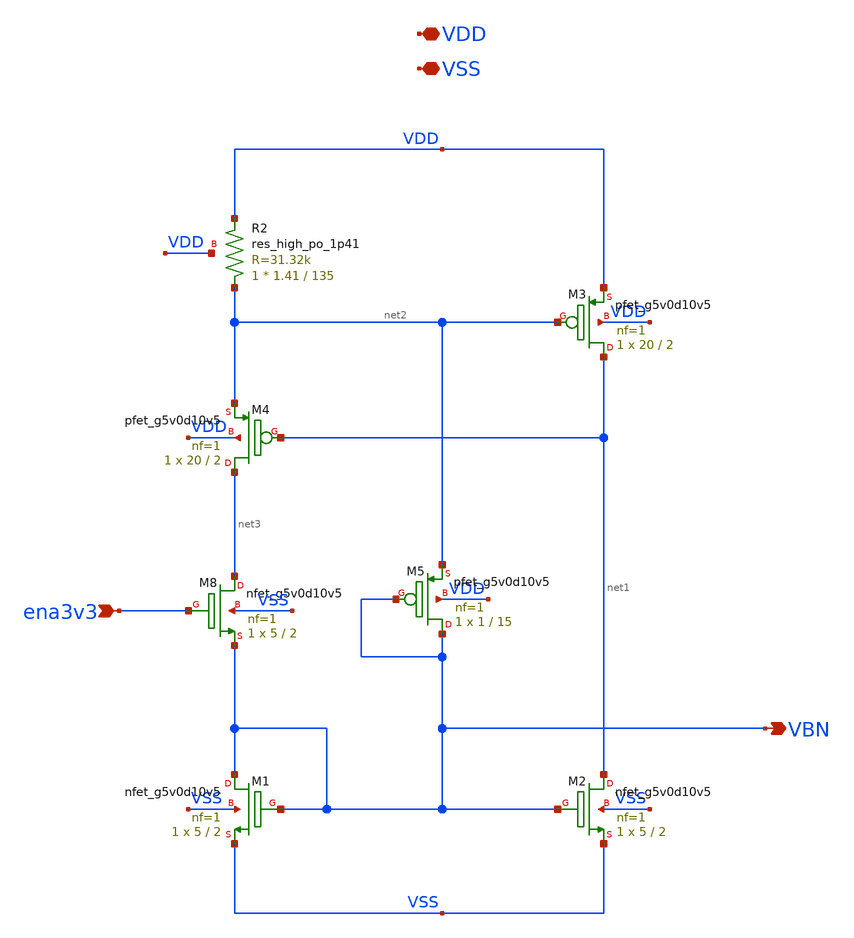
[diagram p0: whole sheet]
** sch_path: xschem/scomp_bias.sch
**.subckt scomp_bias VBN VDD VSS ena3v3
*.opin VBN
*.iopin VDD
*.iopin VSS
*.ipin ena3v3
XM3 net1 net2 VDD VDD sky130_fd_pr__pfet_g5v0d10v5 L=2 W=20 nf=1 ad='int((nf+1)/2) * W/nf * 0.29' as='int((nf+2)/2) * W/nf * 0.29'
+ pd='2*int((nf+1)/2) * (W/nf + 0.29)' ps='2*int((nf+2)/2) * (W/nf + 0.29)' nrd='0.29 / W' nrs='0.29 / W'
+ sa=0 sb=0 sd=0 mult=1 m=1
XM4 net3 net1 net2 VDD sky130_fd_pr__pfet_g5v0d10v5 L=2 W=20 nf=1 ad='int((nf+1)/2) * W/nf * 0.29' as='int((nf+2)/2) * W/nf * 0.29'
+ pd='2*int((nf+1)/2) * (W/nf + 0.29)' ps='2*int((nf+2)/2) * (W/nf + 0.29)' nrd='0.29 / W' nrs='0.29 / W'
+ sa=0 sb=0 sd=0 mult=1 m=1
XM5 VBN VBN net2 VDD sky130_fd_pr__pfet_g5v0d10v5 L=15 W=1 nf=1 ad='int((nf+1)/2) * W/nf * 0.29' as='int((nf+2)/2) * W/nf * 0.29'
+ pd='2*int((nf+1)/2) * (W/nf + 0.29)' ps='2*int((nf+2)/2) * (W/nf + 0.29)' nrd='0.29 / W' nrs='0.29 / W'
+ sa=0 sb=0 sd=0 mult=1 m=1
XM1 VBN VBN VSS VSS sky130_fd_pr__nfet_g5v0d10v5 L=2 W=5 nf=1 ad='int((nf+1)/2) * W/nf * 0.29' as='int((nf+2)/2) * W/nf * 0.29'
+ pd='2*int((nf+1)/2) * (W/nf + 0.29)' ps='2*int((nf+2)/2) * (W/nf + 0.29)' nrd='0.29 / W' nrs='0.29 / W'
+ sa=0 sb=0 sd=0 mult=1 m=1
XM2 net1 VBN VSS VSS sky130_fd_pr__nfet_g5v0d10v5 L=2 W=5 nf=1 ad='int((nf+1)/2) * W/nf * 0.29' as='int((nf+2)/2) * W/nf * 0.29'
+ pd='2*int((nf+1)/2) * (W/nf + 0.29)' ps='2*int((nf+2)/2) * (W/nf + 0.29)' nrd='0.29 / W' nrs='0.29 / W'
+ sa=0 sb=0 sd=0 mult=1 m=1
XM8 net3 ena3v3 VBN VSS sky130_fd_pr__nfet_g5v0d10v5 L=2 W=5 nf=1 ad='int((nf+1)/2) * W/nf * 0.29' as='int((nf+2)/2) * W/nf * 0.29'
+ pd='2*int((nf+1)/2) * (W/nf + 0.29)' ps='2*int((nf+2)/2) * (W/nf + 0.29)' nrd='0.29 / W' nrs='0.29 / W'
+ sa=0 sb=0 sd=0 mult=1 m=1
XR2 net2 VDD VDD sky130_fd_pr__res_high_po_1p41 L=135 mult=1 m=1
**.ends
.end
